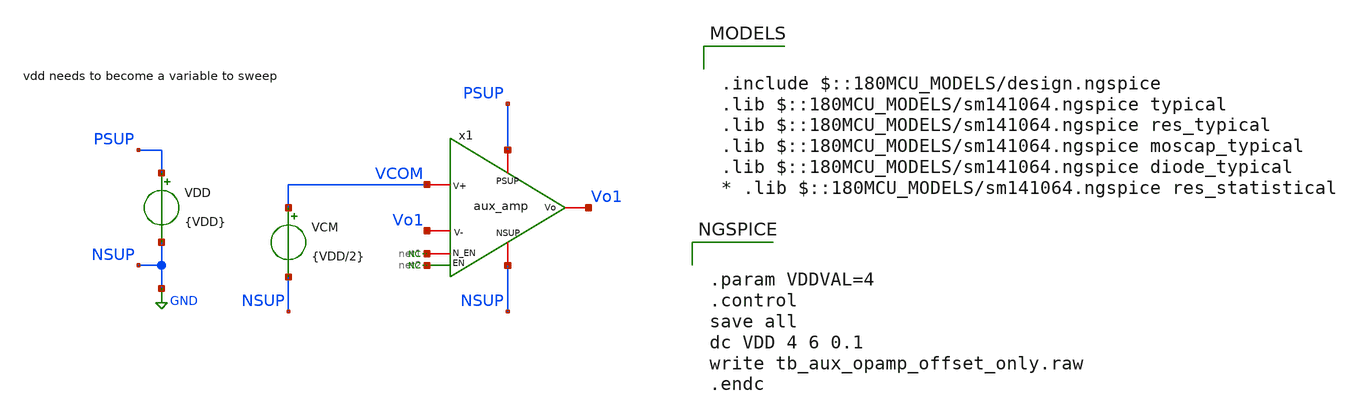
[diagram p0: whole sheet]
** sch_path: xschem/tb/tb_aux_opamp_offset_only.sch
**.subckt tb_aux_opamp_offset_only
x1 PSUP Vo1 VCOM Vo1 net1 NSUP net2 aux_amp
VDD PSUP NSUP {VDD}
VCM VCOM NSUP {VDD/2}
* noconn #net2
* noconn #net1
**** begin user architecture code

.include $::180MCU_MODELS/design.ngspice
.lib $::180MCU_MODELS/sm141064.ngspice typical
.lib $::180MCU_MODELS/sm141064.ngspice res_typical
.lib $::180MCU_MODELS/sm141064.ngspice moscap_typical
.lib $::180MCU_MODELS/sm141064.ngspice diode_typical
* .lib $::180MCU_MODELS/sm141064.ngspice res_statistical



.param VDDVAL=4
.control
save all
dc VDD 4 6 0.1
write tb_aux_opamp_offset_only.raw
.endc


**** end user architecture code
**.ends

* expanding   symbol:  lib/aux_amp.sym # of pins=7
** sym_path: xschem/lib/aux_amp.sym
** sch_path: xschem/lib/aux_amp.sch
.subckt aux_amp PSUP Vo V+ V- N_EN NSUP EN
*.ipin PSUP
*.ipin NSUP
*.ipin N_EN
*.ipin EN
*.ipin V+
*.ipin V-
*.opin Vo
XM1 Vo V- net2 NSUP nfet_06v0 L=0.5u W=2u nf=4 ad='int((nf+1)/2) * W/nf * 0.18u' as='int((nf+2)/2) * W/nf * 0.18u'
+ pd='2*int((nf+1)/2) * (W/nf + 0.18u)' ps='2*int((nf+2)/2) * (W/nf + 0.18u)' nrd='0.18u / W' nrs='0.18u / W'
+ sa=0 sb=0 sd=0 m=4
XM2 net1 V+ net2 NSUP nfet_06v0 L=0.5u W=2u nf=4 ad='int((nf+1)/2) * W/nf * 0.18u' as='int((nf+2)/2) * W/nf * 0.18u'
+ pd='2*int((nf+1)/2) * (W/nf + 0.18u)' ps='2*int((nf+2)/2) * (W/nf + 0.18u)' nrd='0.18u / W' nrs='0.18u / W'
+ sa=0 sb=0 sd=0 m=4
XM5 net1 net1 PSUP PSUP pfet_06v0 L=2u W=2u nf=1 ad='int((nf+1)/2) * W/nf * 0.18u' as='int((nf+2)/2) * W/nf * 0.18u'
+ pd='2*int((nf+1)/2) * (W/nf + 0.18u)' ps='2*int((nf+2)/2) * (W/nf + 0.18u)' nrd='0.18u / W' nrs='0.18u / W'
+ sa=0 sb=0 sd=0 m=1
XM6 Vo net1 PSUP PSUP pfet_06v0 L=2u W=2u nf=1 ad='int((nf+1)/2) * W/nf * 0.18u' as='int((nf+2)/2) * W/nf * 0.18u'
+ pd='2*int((nf+1)/2) * (W/nf + 0.18u)' ps='2*int((nf+2)/2) * (W/nf + 0.18u)' nrd='0.18u / W' nrs='0.18u / W'
+ sa=0 sb=0 sd=0 m=1
I0 net2 NSUP 5u
* noconn N_EN
* noconn EN
.ends

.GLOBAL GND
.end
